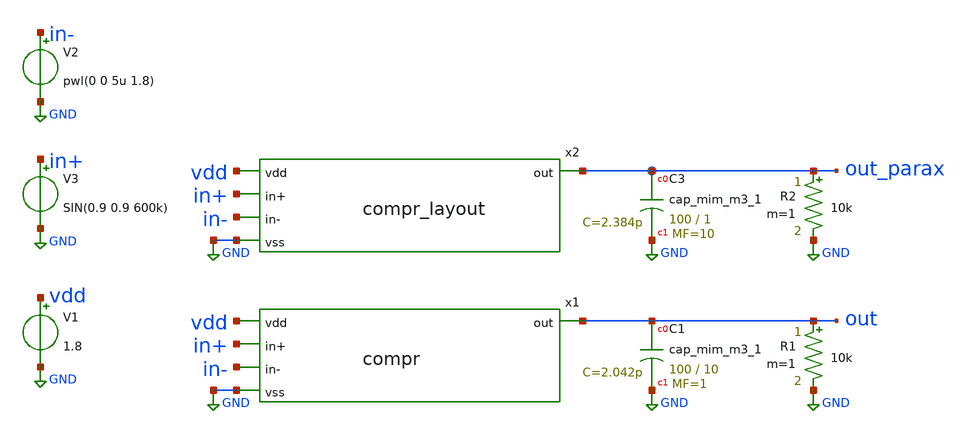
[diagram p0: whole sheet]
** sch_path: custom_gds/tt_um_tim2305_adc_dac/xschem/compr_tb.sch
**.subckt compr_tb
V1 vdd GND 1.8
V3 in+ GND SIN(0.9 0.9 600k)
V2 in- GND pwl(0 0 5u 1.8)
x1 out vdd in+ in- GND compr
x2 out_parax vdd in+ in- GND compr_layout
XC3 out_parax GND sky130_fd_pr__cap_mim_m3_1 W=100 L=1 MF=10 m=10
XC1 out GND sky130_fd_pr__cap_mim_m3_1 W=100 L=10 MF=1 m=1
R1 out GND 10k m=1
R2 out_parax GND 10k m=1
**** begin user architecture code


.tran 100p 5u
.save all
.lib /home/ttuser/pdk/sky130A/libs.tech/ngspice/sky130.lib.spice tt


**** end user architecture code
**.ends

* expanding   symbol:  /home/ttuser/Documents/aprx_adc/compr.sym # of pins=5
** sym_path: custom_gds/tt_um_tim2305_adc_dac/xschem/compr.sym
** sch_path: custom_gds/tt_um_tim2305_adc_dac/xschem/compr.sch
.subckt compr out vdd in+ in- vss
*.ipin in+
*.ipin in-
*.ipin vdd
*.opin out
*.ipin vss
XM3 bias bias vdd vdd sky130_fd_pr__pfet_01v8 L=1 W=8 nf=1 ad='int((nf+1)/2) * W/nf * 0.29' as='int((nf+2)/2) * W/nf * 0.29'
+ pd='2*int((nf+1)/2) * (W/nf + 0.29)' ps='2*int((nf+2)/2) * (W/nf + 0.29)' nrd='0.29 / W' nrs='0.29 / W'
+ sa=0 sb=0 sd=0 mult=1 m=1
XM8 net3 bias vdd vdd sky130_fd_pr__pfet_01v8 L=1 W=8 nf=1 ad='int((nf+1)/2) * W/nf * 0.29' as='int((nf+2)/2) * W/nf * 0.29'
+ pd='2*int((nf+1)/2) * (W/nf + 0.29)' ps='2*int((nf+2)/2) * (W/nf + 0.29)' nrd='0.29 / W' nrs='0.29 / W'
+ sa=0 sb=0 sd=0 mult=1 m=1
XM5 net2 net1 vss vss sky130_fd_pr__nfet_01v8_lvt L=2 W=4 nf=1 ad='int((nf+1)/2) * W/nf * 0.29' as='int((nf+2)/2) * W/nf * 0.29'
+ pd='2*int((nf+1)/2) * (W/nf + 0.29)' ps='2*int((nf+2)/2) * (W/nf + 0.29)' nrd='0.29 / W' nrs='0.29 / W'
+ sa=0 sb=0 sd=0 mult=1 m=1
XM6 net1 net1 vss vss sky130_fd_pr__nfet_01v8_lvt L=2 W=4 nf=1 ad='int((nf+1)/2) * W/nf * 0.29' as='int((nf+2)/2) * W/nf * 0.29'
+ pd='2*int((nf+1)/2) * (W/nf + 0.29)' ps='2*int((nf+2)/2) * (W/nf + 0.29)' nrd='0.29 / W' nrs='0.29 / W'
+ sa=0 sb=0 sd=0 mult=1 m=1
XM7 net1 in- net3 vdd sky130_fd_pr__pfet_01v8_lvt L=2 W=8 nf=1 ad='int((nf+1)/2) * W/nf * 0.29' as='int((nf+2)/2) * W/nf * 0.29'
+ pd='2*int((nf+1)/2) * (W/nf + 0.29)' ps='2*int((nf+2)/2) * (W/nf + 0.29)' nrd='0.29 / W' nrs='0.29 / W'
+ sa=0 sb=0 sd=0 mult=1 m=1
XM9 net2 in+ net3 vdd sky130_fd_pr__pfet_01v8_lvt L=2 W=8 nf=1 ad='int((nf+1)/2) * W/nf * 0.29' as='int((nf+2)/2) * W/nf * 0.29'
+ pd='2*int((nf+1)/2) * (W/nf + 0.29)' ps='2*int((nf+2)/2) * (W/nf + 0.29)' nrd='0.29 / W' nrs='0.29 / W'
+ sa=0 sb=0 sd=0 mult=1 m=1
XM4 bias bias vss vss sky130_fd_pr__nfet_01v8_lvt L=1 W=4 nf=1 ad='int((nf+1)/2) * W/nf * 0.29' as='int((nf+2)/2) * W/nf * 0.29'
+ pd='2*int((nf+1)/2) * (W/nf + 0.29)' ps='2*int((nf+2)/2) * (W/nf + 0.29)' nrd='0.29 / W' nrs='0.29 / W'
+ sa=0 sb=0 sd=0 mult=1 m=1
XM21 out net2 vdd vdd sky130_fd_pr__pfet_01v8 L=0.15 W=3 nf=1 ad='int((nf+1)/2) * W/nf * 0.29' as='int((nf+2)/2) * W/nf * 0.29'
+ pd='2*int((nf+1)/2) * (W/nf + 0.29)' ps='2*int((nf+2)/2) * (W/nf + 0.29)' nrd='0.29 / W' nrs='0.29 / W'
+ sa=0 sb=0 sd=0 mult=1 m=1
XM1 out net2 vss vss sky130_fd_pr__nfet_01v8 L=0.15 W=1 nf=1 ad='int((nf+1)/2) * W/nf * 0.29' as='int((nf+2)/2) * W/nf * 0.29'
+ pd='2*int((nf+1)/2) * (W/nf + 0.29)' ps='2*int((nf+2)/2) * (W/nf + 0.29)' nrd='0.29 / W' nrs='0.29 / W'
+ sa=0 sb=0 sd=0 mult=1 m=1
.ends


* expanding   symbol:  /home/ttuser/Documents/aprx_adc/compr_layout.sym # of pins=5
** sym_path: custom_gds/tt_um_tim2305_adc_dac/xschem/compr.sym
.include [abs_sym_path compr_layout.spice]
.GLOBAL GND
.end
